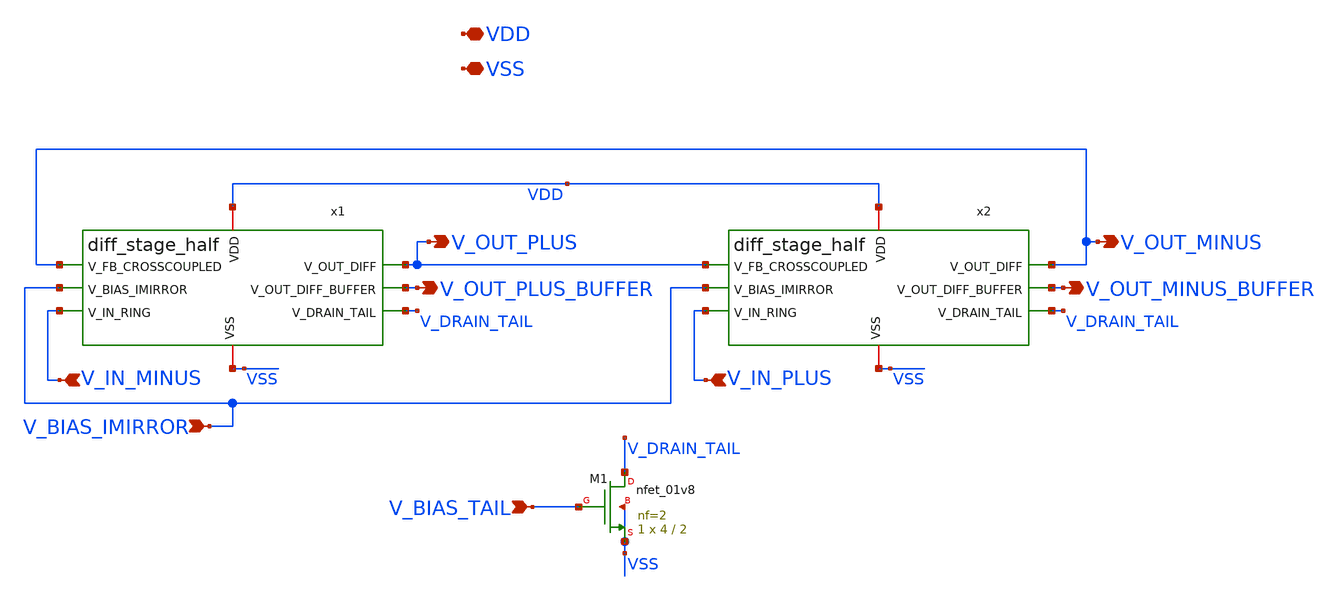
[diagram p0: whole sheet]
** sch_path: xschem/diff_stage.sch
**.subckt diff_stage V_OUT_PLUS V_OUT_PLUS_BUFFER V_OUT_MINUS V_OUT_MINUS_BUFFER V_BIAS_IMIRROR
*+ V_IN_MINUS V_IN_PLUS V_BIAS_TAIL VDD VSS
*.opin V_OUT_PLUS
*.opin V_OUT_PLUS_BUFFER
*.opin V_OUT_MINUS
*.opin V_OUT_MINUS_BUFFER
*.ipin V_BIAS_IMIRROR
*.ipin V_IN_MINUS
*.ipin V_IN_PLUS
*.ipin V_BIAS_TAIL
*.iopin VDD
*.iopin VSS
x1 VDD V_OUT_MINUS V_BIAS_IMIRROR V_OUT_PLUS V_OUT_PLUS_BUFFER V_IN_MINUS VSS V_DRAIN_TAIL
+ diff_stage_half
x2 VDD V_OUT_PLUS V_BIAS_IMIRROR V_OUT_MINUS V_OUT_MINUS_BUFFER V_IN_PLUS VSS V_DRAIN_TAIL
+ diff_stage_half
XM1 V_DRAIN_TAIL V_BIAS_TAIL VSS VSS sky130_fd_pr__nfet_01v8 L=2 W=4 nf=2 ad='int((nf+1)/2) * W/nf * 0.29'
+ as='int((nf+2)/2) * W/nf * 0.29' pd='2*int((nf+1)/2) * (W/nf + 0.29)' ps='2*int((nf+2)/2) * (W/nf + 0.29)'
+ nrd='0.29 / W' nrs='0.29 / W' sa=0 sb=0 sd=0 mult=1 m=1
**.ends

* expanding   symbol:  diff_stage_half.sym # of pins=8
** sym_path: xschem/diff_stage_half.sym
** sch_path: xschem/diff_stage_half.sch
.subckt diff_stage_half VDD V_FB_CROSSCOUPLED V_BIAS_IMIRROR V_OUT_DIFF V_OUT_DIFF_BUFFER V_IN_RING
+ VSS V_DRAIN_TAIL
*.ipin V_BIAS_IMIRROR
*.ipin V_FB_CROSSCOUPLED
*.ipin V_IN_RING
*.opin V_OUT_DIFF
*.iopin VDD
*.iopin VSS
*.opin V_OUT_DIFF_BUFFER
*.iopin V_DRAIN_TAIL
XM1 V_OUT_DIFF V_BIAS_IMIRROR VDD VDD sky130_fd_pr__pfet_01v8 L=2 W=4 nf=2 ad='int((nf+1)/2) * W/nf * 0.29'
+ as='int((nf+2)/2) * W/nf * 0.29' pd='2*int((nf+1)/2) * (W/nf + 0.29)' ps='2*int((nf+2)/2) * (W/nf + 0.29)'
+ nrd='0.29 / W' nrs='0.29 / W' sa=0 sb=0 sd=0 mult=1 m=1
XM2 V_OUT_DIFF V_FB_CROSSCOUPLED VDD VDD sky130_fd_pr__pfet_01v8 L=2 W=4 nf=2 ad='int((nf+1)/2) * W/nf * 0.29'
+ as='int((nf+2)/2) * W/nf * 0.29' pd='2*int((nf+1)/2) * (W/nf + 0.29)' ps='2*int((nf+2)/2) * (W/nf + 0.29)'
+ nrd='0.29 / W' nrs='0.29 / W' sa=0 sb=0 sd=0 mult=1 m=1
XM3 V_OUT_DIFF V_IN_RING V_DRAIN_TAIL VSS sky130_fd_pr__nfet_01v8 L=2 W=4 nf=2 ad='int((nf+1)/2) * W/nf * 0.29'
+ as='int((nf+2)/2) * W/nf * 0.29' pd='2*int((nf+1)/2) * (W/nf + 0.29)' ps='2*int((nf+2)/2) * (W/nf + 0.29)'
+ nrd='0.29 / W' nrs='0.29 / W' sa=0 sb=0 sd=0 mult=1 m=1
XM4 VSS V_OUT_DIFF VSS VSS sky130_fd_pr__nfet_01v8 L=11 W=11 nf=1 ad='int((nf+1)/2) * W/nf * 0.29' as='int((nf+2)/2) * W/nf * 0.29'
+ pd='2*int((nf+1)/2) * (W/nf + 0.29)' ps='2*int((nf+2)/2) * (W/nf + 0.29)' nrd='0.29 / W' nrs='0.29 / W'
+ sa=0 sb=0 sd=0 mult=1 m=1
x1 VDD VSS V_OUT_DIFF_BUFFER V_OUT_DIFF min_buffer
.ends


* expanding   symbol:  min_buffer.sym # of pins=4
** sym_path: xschem/min_buffer.sym
** sch_path: xschem/min_buffer.sch
.subckt min_buffer VDD VSS VOUT_BUFFER VIN_BUFFER
*.ipin VIN_BUFFER
*.opin VOUT_BUFFER
*.iopin VDD
*.iopin VSS
x1 VDD VSS VOUT_BUFFER INT_BUFFER min_inv
x2 VDD VSS INT_BUFFER VIN_BUFFER min_inv
.ends


* expanding   symbol:  min_inv.sym # of pins=4
** sym_path: xschem/min_inv.sym
** sch_path: xschem/min_inv.sch
.subckt min_inv VDD VSS VOUT_INV VIN_INV
*.iopin VDD
*.iopin VSS
*.ipin VIN_INV
*.opin VOUT_INV
XM2 VOUT_INV VIN_INV VSS VSS sky130_fd_pr__nfet_01v8 L=0.15 W=1 nf=1 ad='int((nf+1)/2) * W/nf * 0.29'
+ as='int((nf+2)/2) * W/nf * 0.29' pd='2*int((nf+1)/2) * (W/nf + 0.29)' ps='2*int((nf+2)/2) * (W/nf + 0.29)'
+ nrd='0.29 / W' nrs='0.29 / W' sa=0 sb=0 sd=0 mult=1 m=1
XM3 VOUT_INV VIN_INV VDD VDD sky130_fd_pr__pfet_01v8 L=0.15 W=1 nf=1 ad='int((nf+1)/2) * W/nf * 0.29'
+ as='int((nf+2)/2) * W/nf * 0.29' pd='2*int((nf+1)/2) * (W/nf + 0.29)' ps='2*int((nf+2)/2) * (W/nf + 0.29)'
+ nrd='0.29 / W' nrs='0.29 / W' sa=0 sb=0 sd=0 mult=1 m=1
.ends

.end
